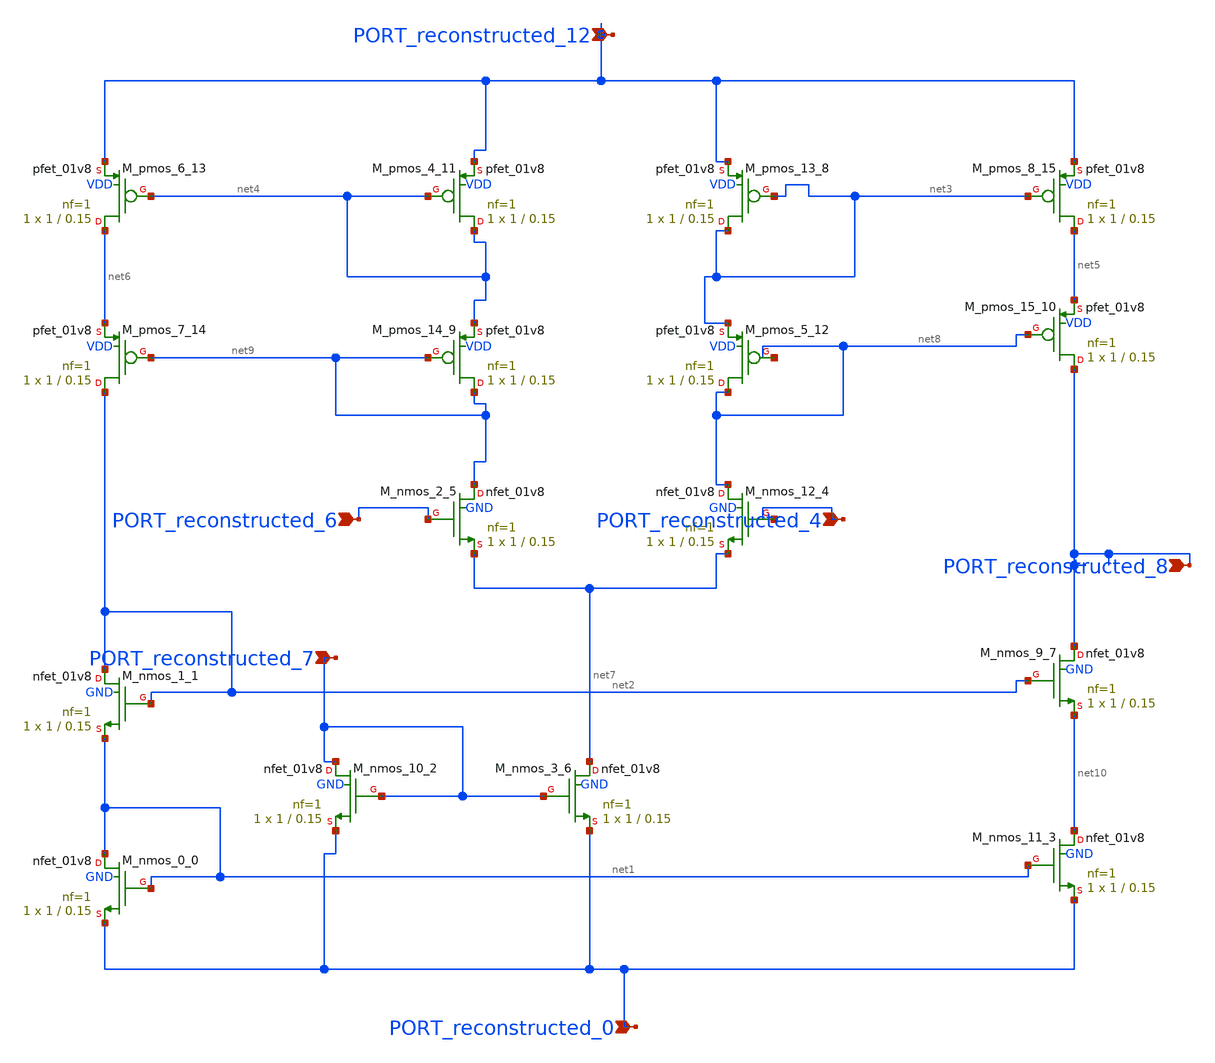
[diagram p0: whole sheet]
** sch_path: schematics/Image2Net/054.sch
**.subckt 054 PORT_reconstructed_7 PORT_reconstructed_6 PORT_reconstructed_0 PORT_reconstructed_4
*+ PORT_reconstructed_8 PORT_reconstructed_12
*.ipin PORT_reconstructed_7
*.ipin PORT_reconstructed_6
*.ipin PORT_reconstructed_0
*.ipin PORT_reconstructed_4
*.ipin PORT_reconstructed_8
*.ipin PORT_reconstructed_12
XM_nmos_0_0 net1 net1 PORT_reconstructed_0 GND sky130_fd_pr__nfet_01v8 L=0.15 W=1 nf=1 ad='int((1 + 1)/2) * 1 / 1 * 0.29'
+ as='int((1 + 2)/2) * 1 / 1 * 0.29' pd='2*int((1 + 1)/2) * (1 / 1 + 0.29)' ps='2*int((1 + 2)/2) * (1 / 1 + 0.29)'
+ nrd='0.29 / 1 ' nrs='0.29 / 1 ' sa=0 sb=0 sd=0 mult=1 m=1
XM_nmos_1_1 net2 net2 net1 GND sky130_fd_pr__nfet_01v8 L=0.15 W=1 nf=1 ad='int((1 + 1)/2) * 1 / 1 * 0.29'
+ as='int((1 + 2)/2) * 1 / 1 * 0.29' pd='2*int((1 + 1)/2) * (1 / 1 + 0.29)' ps='2*int((1 + 2)/2) * (1 / 1 + 0.29)'
+ nrd='0.29 / 1 ' nrs='0.29 / 1 ' sa=0 sb=0 sd=0 mult=1 m=1
XM_nmos_10_2 PORT_reconstructed_7 PORT_reconstructed_7 PORT_reconstructed_0 GND sky130_fd_pr__nfet_01v8
+ L=0.15 W=1 nf=1 ad='int((1 + 1)/2) * 1 / 1 * 0.29' as='int((1 + 2)/2) * 1 / 1 * 0.29' pd='2*int((1 + 1)/2) * (1 / 1 + 0.29)'
+ ps='2*int((1 + 2)/2) * (1 / 1 + 0.29)' nrd='0.29 / 1 ' nrs='0.29 / 1 ' sa=0 sb=0 sd=0 mult=1 m=1
XM_nmos_11_3 net10 net1 PORT_reconstructed_0 GND sky130_fd_pr__nfet_01v8 L=0.15 W=1 nf=1 ad='int((1 + 1)/2) * 1 / 1 * 0.29'
+ as='int((1 + 2)/2) * 1 / 1 * 0.29' pd='2*int((1 + 1)/2) * (1 / 1 + 0.29)' ps='2*int((1 + 2)/2) * (1 / 1 + 0.29)'
+ nrd='0.29 / 1 ' nrs='0.29 / 1 ' sa=0 sb=0 sd=0 mult=1 m=1
XM_nmos_12_4 net8 PORT_reconstructed_4 net7 GND sky130_fd_pr__nfet_01v8 L=0.15 W=1 nf=1 ad='int((1 + 1)/2) * 1 / 1 * 0.29'
+ as='int((1 + 2)/2) * 1 / 1 * 0.29' pd='2*int((1 + 1)/2) * (1 / 1 + 0.29)' ps='2*int((1 + 2)/2) * (1 / 1 + 0.29)'
+ nrd='0.29 / 1 ' nrs='0.29 / 1 ' sa=0 sb=0 sd=0 mult=1 m=1
XM_nmos_2_5 net9 PORT_reconstructed_6 net7 GND sky130_fd_pr__nfet_01v8 L=0.15 W=1 nf=1 ad='int((1 + 1)/2) * 1 / 1 * 0.29'
+ as='int((1 + 2)/2) * 1 / 1 * 0.29' pd='2*int((1 + 1)/2) * (1 / 1 + 0.29)' ps='2*int((1 + 2)/2) * (1 / 1 + 0.29)'
+ nrd='0.29 / 1 ' nrs='0.29 / 1 ' sa=0 sb=0 sd=0 mult=1 m=1
XM_nmos_3_6 net7 PORT_reconstructed_7 PORT_reconstructed_0 GND sky130_fd_pr__nfet_01v8 L=0.15 W=1 nf=1
+ ad='int((1 + 1)/2) * 1 / 1 * 0.29' as='int((1 + 2)/2) * 1 / 1 * 0.29' pd='2*int((1 + 1)/2) * (1 / 1 + 0.29)'
+ ps='2*int((1 + 2)/2) * (1 / 1 + 0.29)' nrd='0.29 / 1 ' nrs='0.29 / 1 ' sa=0 sb=0 sd=0 mult=1 m=1
XM_nmos_9_7 PORT_reconstructed_8 net2 net10 GND sky130_fd_pr__nfet_01v8 L=0.15 W=1 nf=1 ad='int((1 + 1)/2) * 1 / 1 * 0.29'
+ as='int((1 + 2)/2) * 1 / 1 * 0.29' pd='2*int((1 + 1)/2) * (1 / 1 + 0.29)' ps='2*int((1 + 2)/2) * (1 / 1 + 0.29)'
+ nrd='0.29 / 1 ' nrs='0.29 / 1 ' sa=0 sb=0 sd=0 mult=1 m=1
XM_pmos_13_8 net3 net3 PORT_reconstructed_12 VDD sky130_fd_pr__pfet_01v8 L=0.15 W=1 nf=1 ad='int((1 + 1)/2) * 1 / 1 * 0.29'
+ as='int((1 + 2)/2) * 1 / 1 * 0.29' pd='2*int((1 + 1)/2) * (1 / 1 + 0.29)' ps='2*int((1 + 2)/2) * (1 / 1 + 0.29)'
+ nrd='0.29 / 1 ' nrs='0.29 / 1 ' sa=0 sb=0 sd=0 mult=1 m=1
XM_pmos_14_9 net9 net9 net4 VDD sky130_fd_pr__pfet_01v8 L=0.15 W=1 nf=1 ad='int((1 + 1)/2) * 1 / 1 * 0.29'
+ as='int((1 + 2)/2) * 1 / 1 * 0.29' pd='2*int((1 + 1)/2) * (1 / 1 + 0.29)' ps='2*int((1 + 2)/2) * (1 / 1 + 0.29)'
+ nrd='0.29 / 1 ' nrs='0.29 / 1 ' sa=0 sb=0 sd=0 mult=1 m=1
XM_pmos_15_10 PORT_reconstructed_8 net8 net5 VDD sky130_fd_pr__pfet_01v8 L=0.15 W=1 nf=1 ad='int((1 + 1)/2) * 1 / 1 * 0.29'
+ as='int((1 + 2)/2) * 1 / 1 * 0.29' pd='2*int((1 + 1)/2) * (1 / 1 + 0.29)' ps='2*int((1 + 2)/2) * (1 / 1 + 0.29)'
+ nrd='0.29 / 1 ' nrs='0.29 / 1 ' sa=0 sb=0 sd=0 mult=1 m=1
XM_pmos_4_11 net4 net4 PORT_reconstructed_12 VDD sky130_fd_pr__pfet_01v8 L=0.15 W=1 nf=1 ad='int((1 + 1)/2) * 1 / 1 * 0.29'
+ as='int((1 + 2)/2) * 1 / 1 * 0.29' pd='2*int((1 + 1)/2) * (1 / 1 + 0.29)' ps='2*int((1 + 2)/2) * (1 / 1 + 0.29)'
+ nrd='0.29 / 1 ' nrs='0.29 / 1 ' sa=0 sb=0 sd=0 mult=1 m=1
XM_pmos_5_12 net8 net8 net3 VDD sky130_fd_pr__pfet_01v8 L=0.15 W=1 nf=1 ad='int((1 + 1)/2) * 1 / 1 * 0.29'
+ as='int((1 + 2)/2) * 1 / 1 * 0.29' pd='2*int((1 + 1)/2) * (1 / 1 + 0.29)' ps='2*int((1 + 2)/2) * (1 / 1 + 0.29)'
+ nrd='0.29 / 1 ' nrs='0.29 / 1 ' sa=0 sb=0 sd=0 mult=1 m=1
XM_pmos_6_13 net6 net4 PORT_reconstructed_12 VDD sky130_fd_pr__pfet_01v8 L=0.15 W=1 nf=1 ad='int((1 + 1)/2) * 1 / 1 * 0.29'
+ as='int((1 + 2)/2) * 1 / 1 * 0.29' pd='2*int((1 + 1)/2) * (1 / 1 + 0.29)' ps='2*int((1 + 2)/2) * (1 / 1 + 0.29)'
+ nrd='0.29 / 1 ' nrs='0.29 / 1 ' sa=0 sb=0 sd=0 mult=1 m=1
XM_pmos_7_14 net2 net9 net6 VDD sky130_fd_pr__pfet_01v8 L=0.15 W=1 nf=1 ad='int((1 + 1)/2) * 1 / 1 * 0.29'
+ as='int((1 + 2)/2) * 1 / 1 * 0.29' pd='2*int((1 + 1)/2) * (1 / 1 + 0.29)' ps='2*int((1 + 2)/2) * (1 / 1 + 0.29)'
+ nrd='0.29 / 1 ' nrs='0.29 / 1 ' sa=0 sb=0 sd=0 mult=1 m=1
XM_pmos_8_15 net5 net3 PORT_reconstructed_12 VDD sky130_fd_pr__pfet_01v8 L=0.15 W=1 nf=1 ad='int((1 + 1)/2) * 1 / 1 * 0.29'
+ as='int((1 + 2)/2) * 1 / 1 * 0.29' pd='2*int((1 + 1)/2) * (1 / 1 + 0.29)' ps='2*int((1 + 2)/2) * (1 / 1 + 0.29)'
+ nrd='0.29 / 1 ' nrs='0.29 / 1 ' sa=0 sb=0 sd=0 mult=1 m=1
**.ends
.end
